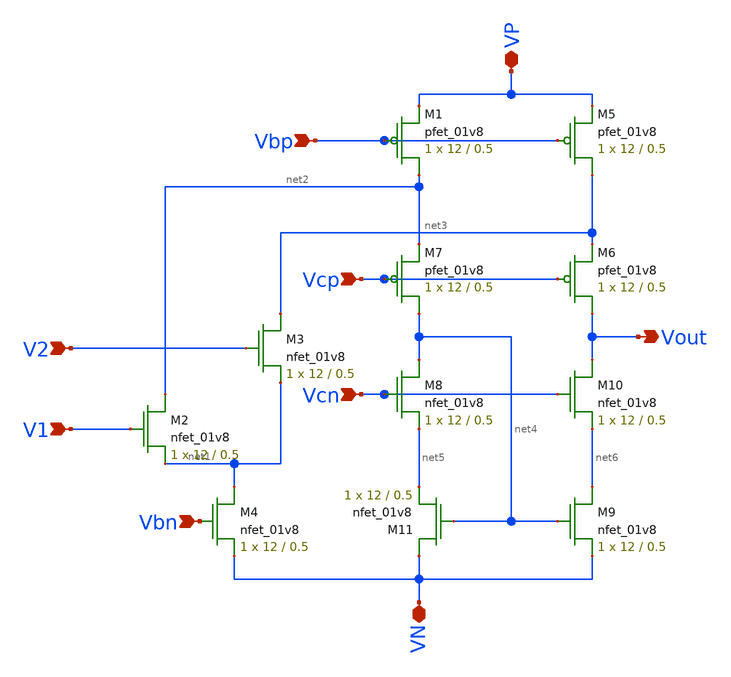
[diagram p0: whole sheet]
** sch_path: mp3/schematic/fcda.sch
**.subckt fcda VP VN Vbp V2 V1 Vbn Vcp Vcn Vout
*.iopin VP
*.iopin VN
*.ipin Vbp
*.ipin V2
*.ipin V1
*.ipin Vbn
*.ipin Vcp
*.ipin Vcn
*.opin Vout
XM1 net2 Vbp VP VDD sky130_fd_pr__pfet_01v8 L=0.5 W=12 nf=1 ad='int((nf+1)/2) * W/nf * 0.29' as='int((nf+2)/2) * W/nf * 0.29'
+ pd='2*int((nf+1)/2) * (W/nf + 0.29)' ps='2*int((nf+2)/2) * (W/nf + 0.29)' nrd='0.29 / W' nrs='0.29 / W'
+ sa=0 sb=0 sd=0 mult=1 m=1
XM2 net2 V1 net1 GND sky130_fd_pr__nfet_01v8 L=0.5 W=12 nf=1 ad='int((nf+1)/2) * W/nf * 0.29' as='int((nf+2)/2) * W/nf * 0.29'
+ pd='2*int((nf+1)/2) * (W/nf + 0.29)' ps='2*int((nf+2)/2) * (W/nf + 0.29)' nrd='0.29 / W' nrs='0.29 / W'
+ sa=0 sb=0 sd=0 mult=1 m=1
XM3 net3 V2 net1 GND sky130_fd_pr__nfet_01v8 L=0.5 W=12 nf=1 ad='int((nf+1)/2) * W/nf * 0.29' as='int((nf+2)/2) * W/nf * 0.29'
+ pd='2*int((nf+1)/2) * (W/nf + 0.29)' ps='2*int((nf+2)/2) * (W/nf + 0.29)' nrd='0.29 / W' nrs='0.29 / W'
+ sa=0 sb=0 sd=0 mult=1 m=1
XM4 net1 Vbn VN GND sky130_fd_pr__nfet_01v8 L=0.5 W=12 nf=1 ad='int((nf+1)/2) * W/nf * 0.29' as='int((nf+2)/2) * W/nf * 0.29'
+ pd='2*int((nf+1)/2) * (W/nf + 0.29)' ps='2*int((nf+2)/2) * (W/nf + 0.29)' nrd='0.29 / W' nrs='0.29 / W'
+ sa=0 sb=0 sd=0 mult=1 m=1
XM5 net3 Vbp VP VDD sky130_fd_pr__pfet_01v8 L=0.5 W=12 nf=1 ad='int((nf+1)/2) * W/nf * 0.29' as='int((nf+2)/2) * W/nf * 0.29'
+ pd='2*int((nf+1)/2) * (W/nf + 0.29)' ps='2*int((nf+2)/2) * (W/nf + 0.29)' nrd='0.29 / W' nrs='0.29 / W'
+ sa=0 sb=0 sd=0 mult=1 m=1
XM6 Vout Vcp net3 VDD sky130_fd_pr__pfet_01v8 L=0.5 W=12 nf=1 ad='int((nf+1)/2) * W/nf * 0.29' as='int((nf+2)/2) * W/nf * 0.29'
+ pd='2*int((nf+1)/2) * (W/nf + 0.29)' ps='2*int((nf+2)/2) * (W/nf + 0.29)' nrd='0.29 / W' nrs='0.29 / W'
+ sa=0 sb=0 sd=0 mult=1 m=1
XM7 net4 Vcp net2 VDD sky130_fd_pr__pfet_01v8 L=0.5 W=12 nf=1 ad='int((nf+1)/2) * W/nf * 0.29' as='int((nf+2)/2) * W/nf * 0.29'
+ pd='2*int((nf+1)/2) * (W/nf + 0.29)' ps='2*int((nf+2)/2) * (W/nf + 0.29)' nrd='0.29 / W' nrs='0.29 / W'
+ sa=0 sb=0 sd=0 mult=1 m=1
XM8 net4 Vcn net5 GND sky130_fd_pr__nfet_01v8 L=0.5 W=12 nf=1 ad='int((nf+1)/2) * W/nf * 0.29' as='int((nf+2)/2) * W/nf * 0.29'
+ pd='2*int((nf+1)/2) * (W/nf + 0.29)' ps='2*int((nf+2)/2) * (W/nf + 0.29)' nrd='0.29 / W' nrs='0.29 / W'
+ sa=0 sb=0 sd=0 mult=1 m=1
XM9 net6 net4 VN GND sky130_fd_pr__nfet_01v8 L=0.5 W=12 nf=1 ad='int((nf+1)/2) * W/nf * 0.29' as='int((nf+2)/2) * W/nf * 0.29'
+ pd='2*int((nf+1)/2) * (W/nf + 0.29)' ps='2*int((nf+2)/2) * (W/nf + 0.29)' nrd='0.29 / W' nrs='0.29 / W'
+ sa=0 sb=0 sd=0 mult=1 m=1
XM10 Vout Vcn net6 GND sky130_fd_pr__nfet_01v8 L=0.5 W=12 nf=1 ad='int((nf+1)/2) * W/nf * 0.29' as='int((nf+2)/2) * W/nf * 0.29'
+ pd='2*int((nf+1)/2) * (W/nf + 0.29)' ps='2*int((nf+2)/2) * (W/nf + 0.29)' nrd='0.29 / W' nrs='0.29 / W'
+ sa=0 sb=0 sd=0 mult=1 m=1
XM11 VN net4 net5 GND sky130_fd_pr__nfet_01v8 L=0.5 W=12 nf=1 ad='int((nf+1)/2) * W/nf * 0.29' as='int((nf+2)/2) * W/nf * 0.29'
+ pd='2*int((nf+1)/2) * (W/nf + 0.29)' ps='2*int((nf+2)/2) * (W/nf + 0.29)' nrd='0.29 / W' nrs='0.29 / W'
+ sa=0 sb=0 sd=0 mult=1 m=1
**.ends
.end
